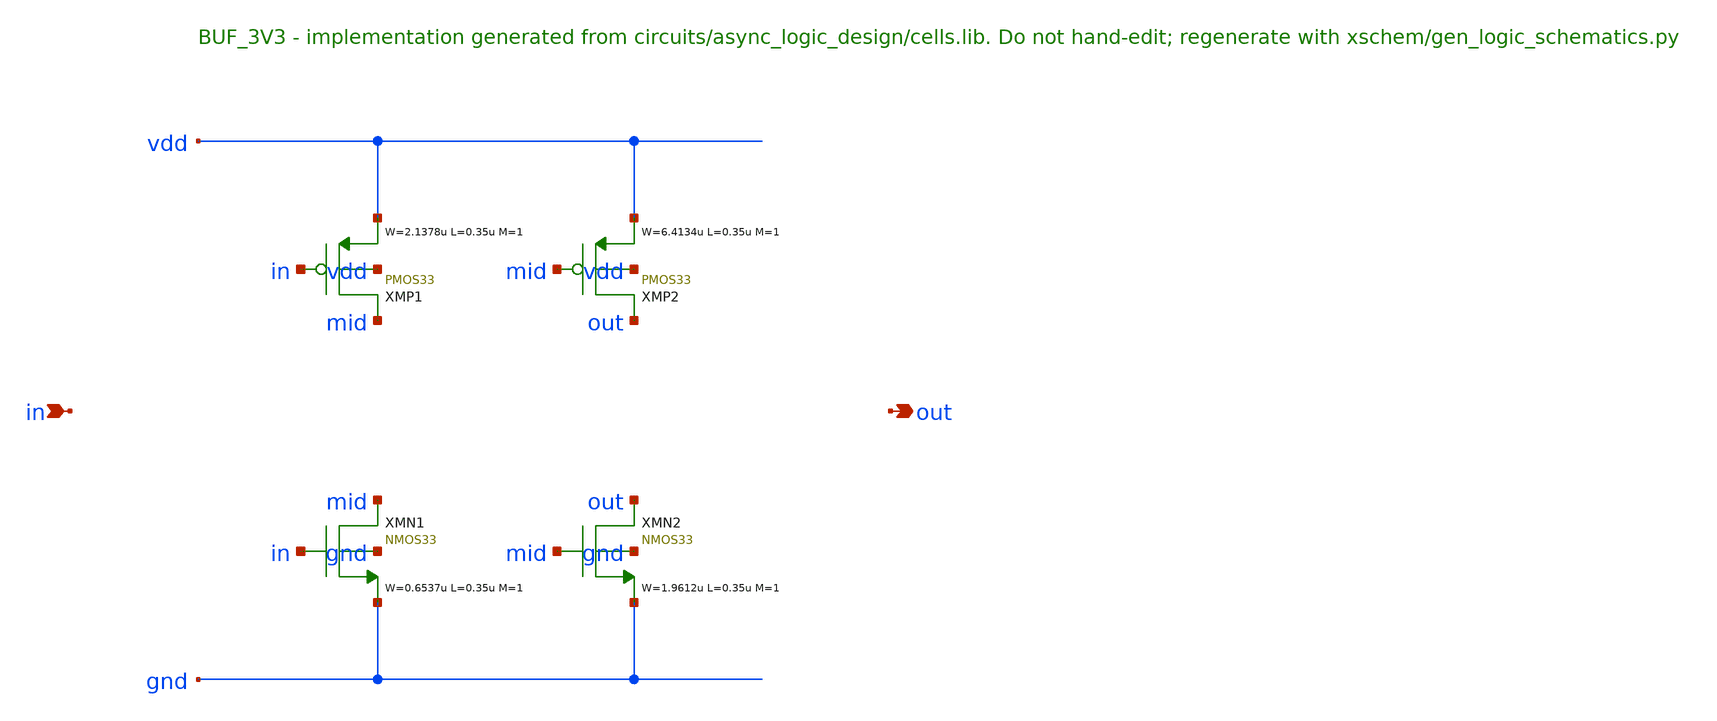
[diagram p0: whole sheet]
** sch_path: xschem/logic/BUF_3V3.sch
**.subckt BUF_3V3 in out
*.ipin in
*.opin out
XMP1 mid in vdd vdd PMOS33 W=2.1378u L=0.35u M=1 MM_SIGMA=0
XMP2 out mid vdd vdd PMOS33 W=6.4134u L=0.35u M=1 MM_SIGMA=0
XMN1 mid in gnd gnd NMOS33 W=0.6537u L=0.35u M=1 MM_SIGMA=0
XMN2 out mid gnd gnd NMOS33 W=1.9612u L=0.35u M=1 MM_SIGMA=0
**.ends
.end
